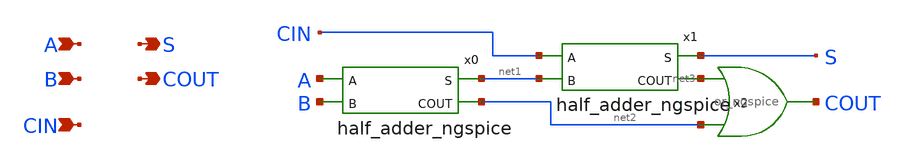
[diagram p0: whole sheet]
** sch_path: xschem-src/xschem_library/ngspice/full_adder_ngspice.sch
* Copyright (C) 1998-2026 Stefan Frederik Schippers
* This program is free software; you can redistribute it and/or modify
* it under the terms of the GNU General Public License as published by
* the Free Software Foundation; either version 2 of the License, or
* (at your option) any later version.
* This program is distributed in the hope that it will be useful,
* but WITHOUT ANY WARRANTY; without even the implied warranty of
* MERCHANTABILITY or FITNESS FOR A PARTICULAR PURPOSE.  See the
* GNU General Public License for more details.
* You should have received a copy of the GNU General Public License
* along with this program; if not, write to the Free Software
**.subckt full_adder_ngspice A B CIN S COUT
*.ipin A
*.ipin B
*.ipin CIN
*.opin S
*.opin COUT
x0 A net1 net2 B half_adder_ngspice
x1 CIN S net3 net1 half_adder_ngspice
x2 COUT net3 net2 or_ngspice ROUT=1000
**.ends

* expanding   symbol:  half_adder_ngspice.sym # of pins=4
** sym_path: xschem-src/xschem_library/ngspice/half_adder_ngspice.sym
** sch_path: xschem-src/xschem_library/ngspice/half_adder_ngspice.sch
.subckt half_adder_ngspice A S COUT B
*.ipin A
*.ipin B
*.opin S
*.opin COUT
x1 S A B xor_ngspice ROUT=1000
x2 COUT A B and_ngspice ROUT=1000
.ends


* expanding   symbol:  or_ngspice.sym # of pins=3
** sym_path: xschem-src/xschem_library/ngspice/or_ngspice.sym
** sch_path: xschem-src/xschem_library/ngspice/or_ngspice.sch
.subckt or_ngspice Y A B  ROUT=1000
*.ipin A
*.opin Y
*.ipin B
B1 net1 0 V = 'VCC/2*(1+tanh((max(V(A1),V(B1))-VCC/2)*100))'
R1 Y1 net1 'ROUT' m=1
C1 A1 0 8f m=1
C2 B1 0 8f m=1
C3 Y1 0 8f m=1
V1 A1 A 0
V2 B1 B 0
V3 Y Y1 0
.ends


* expanding   symbol:  xor_ngspice.sym # of pins=3
** sym_path: xschem-src/xschem_library/ngspice/xor_ngspice.sym
** sch_path: xschem-src/xschem_library/ngspice/xor_ngspice.sch
.subckt xor_ngspice Y A B  ROUT=1000
*.ipin A
*.opin Y
*.ipin B
B1 net1 0 V = 'VCC/2*(1+tanh((abs(V(A1)-V(B1))-VCC/2)*100))'
R1 Y1 net1 'ROUT' m=1
C1 A1 0 8f m=1
C2 B1 0 8f m=1
C3 Y1 0 8f m=1
V1 A1 A 0
V2 B1 B 0
V3 Y Y1 0
.ends


* expanding   symbol:  and_ngspice.sym # of pins=3
** sym_path: xschem-src/xschem_library/ngspice/and_ngspice.sym
** sch_path: xschem-src/xschem_library/ngspice/and_ngspice.sch
.subckt and_ngspice Y A B  ROUT=1000
*.ipin A
*.opin Y
*.ipin B
B1 net1 0 V = 'VCC/2*(1+tanh((min(V(A1),V(B1))-VCC/2)*100))'
R1 Y1 net1 'ROUT' m=1
C1 A1 0 8f m=1
C2 B1 0 8f m=1
C3 Y1 0 8f m=1
V1 A1 A 0
V2 B1 B 0
V3 Y Y1 0
.ends

.end
